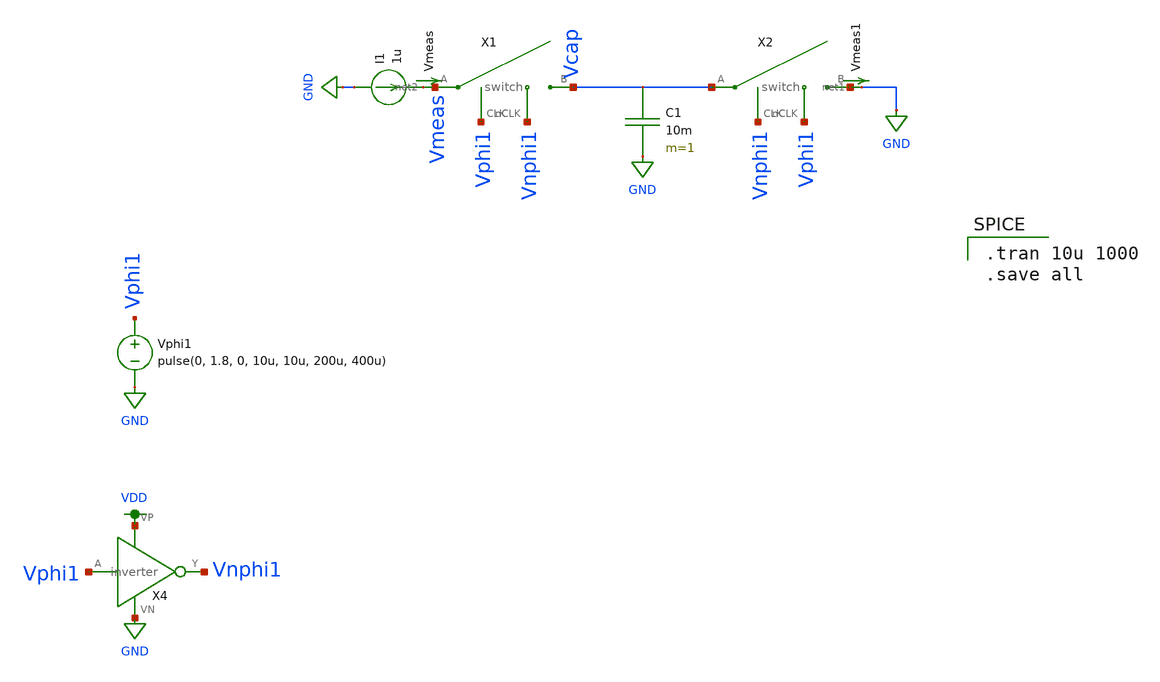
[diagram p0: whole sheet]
** sch_path: switched_capacitor_resistor.sch
**.subckt switched_capacitor_resistor
X1 Vcap Vmeas Vphi1 Vnphi1 switch
C1 Vcap GND 10m m=1
X2 net1 Vcap Vnphi1 Vphi1 switch
Vphi1 Vphi1 GND pulse(0, 1.8, 0, 10u, 10u, 200u, 400u)
X4 Vphi1 Vnphi1 VDD GND inverter
Vmeas net2 Vmeas 0
.save i(vmeas)
Vmeas1 net1 GND 0
.save i(vmeas1)
I1 GND net2 1u
**** begin user architecture code

.option wnflag=1
.param MC_SWITCH=0.0
.lib ~/skywater/skywater-pdk/libraries/sky130_fd_pr_ngspice/latest/models/sky130.lib.spice tt


.tran 10u 1000
.save all

**** end user architecture code
**.ends

* expanding   symbol:  /home/madvlsi/Documents/MADVLSI-Final_Project/schematic/switch.sym # of
*+ pins=4
** sym_path: schematic/switch.sym
** sch_path: schematic/switch.sch
.subckt switch B A CLK nCLK
*.iopin B
*.iopin A
*.ipin CLK
*.ipin nCLK
*.ipin CLK
*.ipin CLK
*.ipin nCLK
*.ipin nCLK
XM1 A CLK B GND sky130_fd_pr__nfet_01v8 L={LL} W={WW} nf=1 ad='int((nf+1)/2) * W/nf * 0.29' as='int((nf+2)/2) * W/nf * 0.29'
+ pd='2*int((nf+1)/2) * (W/nf + 0.29)' ps='2*int((nf+2)/2) * (W/nf + 0.29)' nrd='0.29 / W' nrs='0.29 / W'
+ sa=0 sb=0 sd=0 mult=1 m=1
XM2 A nCLK B VDD sky130_fd_pr__pfet_01v8 L={Lp} W={Wp} nf=1 ad='int((nf+1)/2) * W/nf * 0.29' as='int((nf+2)/2) * W/nf * 0.29'
+ pd='2*int((nf+1)/2) * (W/nf + 0.29)' ps='2*int((nf+2)/2) * (W/nf + 0.29)' nrd='0.29 / W' nrs='0.29 / W'
+ sa=0 sb=0 sd=0 mult=1 m=1
XM3 B CLK B VDD sky130_fd_pr__pfet_01v8 L={Lp} W={Wp/2} nf=1 ad='int((nf+1)/2) * W/nf * 0.29' as='int((nf+2)/2) * W/nf * 0.29'
+ pd='2*int((nf+1)/2) * (W/nf + 0.29)' ps='2*int((nf+2)/2) * (W/nf + 0.29)' nrd='0.29 / W' nrs='0.29 / W'
+ sa=0 sb=0 sd=0 mult=1 m=1
XM4 A CLK A VDD sky130_fd_pr__pfet_01v8 L={Lp} W={Wp/2} nf=1 ad='int((nf+1)/2) * W/nf * 0.29' as='int((nf+2)/2) * W/nf * 0.29'
+ pd='2*int((nf+1)/2) * (W/nf + 0.29)' ps='2*int((nf+2)/2) * (W/nf + 0.29)' nrd='0.29 / W' nrs='0.29 / W'
+ sa=0 sb=0 sd=0 mult=1 m=1
XM5 B nCLK B GND sky130_fd_pr__nfet_01v8 L={LL} W={WW/2} nf=1 ad='int((nf+1)/2) * W/nf * 0.29' as='int((nf+2)/2) * W/nf * 0.29'
+ pd='2*int((nf+1)/2) * (W/nf + 0.29)' ps='2*int((nf+2)/2) * (W/nf + 0.29)' nrd='0.29 / W' nrs='0.29 / W'
+ sa=0 sb=0 sd=0 mult=1 m=1
XM6 A nCLK A GND sky130_fd_pr__nfet_01v8 L={LL} W={WW/2} nf=1 ad='int((nf+1)/2) * W/nf * 0.29' as='int((nf+2)/2) * W/nf * 0.29'
+ pd='2*int((nf+1)/2) * (W/nf + 0.29)' ps='2*int((nf+2)/2) * (W/nf + 0.29)' nrd='0.29 / W' nrs='0.29 / W'
+ sa=0 sb=0 sd=0 mult=1 m=1
.ends


* expanding   symbol:  /home/madvlsi/Documents/MADVLSI-Final_Project/schematic/inverter.sym # of
*+ pins=4
** sym_path: schematic/inverter.sym
** sch_path: schematic/inverter.sch
.subckt inverter A Y VP VN
*.opin Y
*.ipin A
*.iopin VP
*.iopin VN
XM3 Y A VP VDD sky130_fd_pr__pfet_01v8 L={Lp} W={Wp} nf=1 ad='int((nf+1)/2) * W/nf * 0.29' as='int((nf+2)/2) * W/nf * 0.29'
+ pd='2*int((nf+1)/2) * (W/nf + 0.29)' ps='2*int((nf+2)/2) * (W/nf + 0.29)' nrd='0.29 / W' nrs='0.29 / W'
+ sa=0 sb=0 sd=0 mult=1 m=1
XM4 Y A VP VDD sky130_fd_pr__pfet_01v8 L={Lp} W={Wp} nf=1 ad='int((nf+1)/2) * W/nf * 0.29' as='int((nf+2)/2) * W/nf * 0.29'
+ pd='2*int((nf+1)/2) * (W/nf + 0.29)' ps='2*int((nf+2)/2) * (W/nf + 0.29)' nrd='0.29 / W' nrs='0.29 / W'
+ sa=0 sb=0 sd=0 mult=1 m=1
XM5 Y A VN GND sky130_fd_pr__nfet_01v8 L={Lp} W={Wp} nf=1 ad='int((nf+1)/2) * W/nf * 0.29' as='int((nf+2)/2) * W/nf * 0.29'
+ pd='2*int((nf+1)/2) * (W/nf + 0.29)' ps='2*int((nf+2)/2) * (W/nf + 0.29)' nrd='0.29 / W' nrs='0.29 / W'
+ sa=0 sb=0 sd=0 mult=1 m=1
.ends

.GLOBAL GND
.GLOBAL VDD
.end
